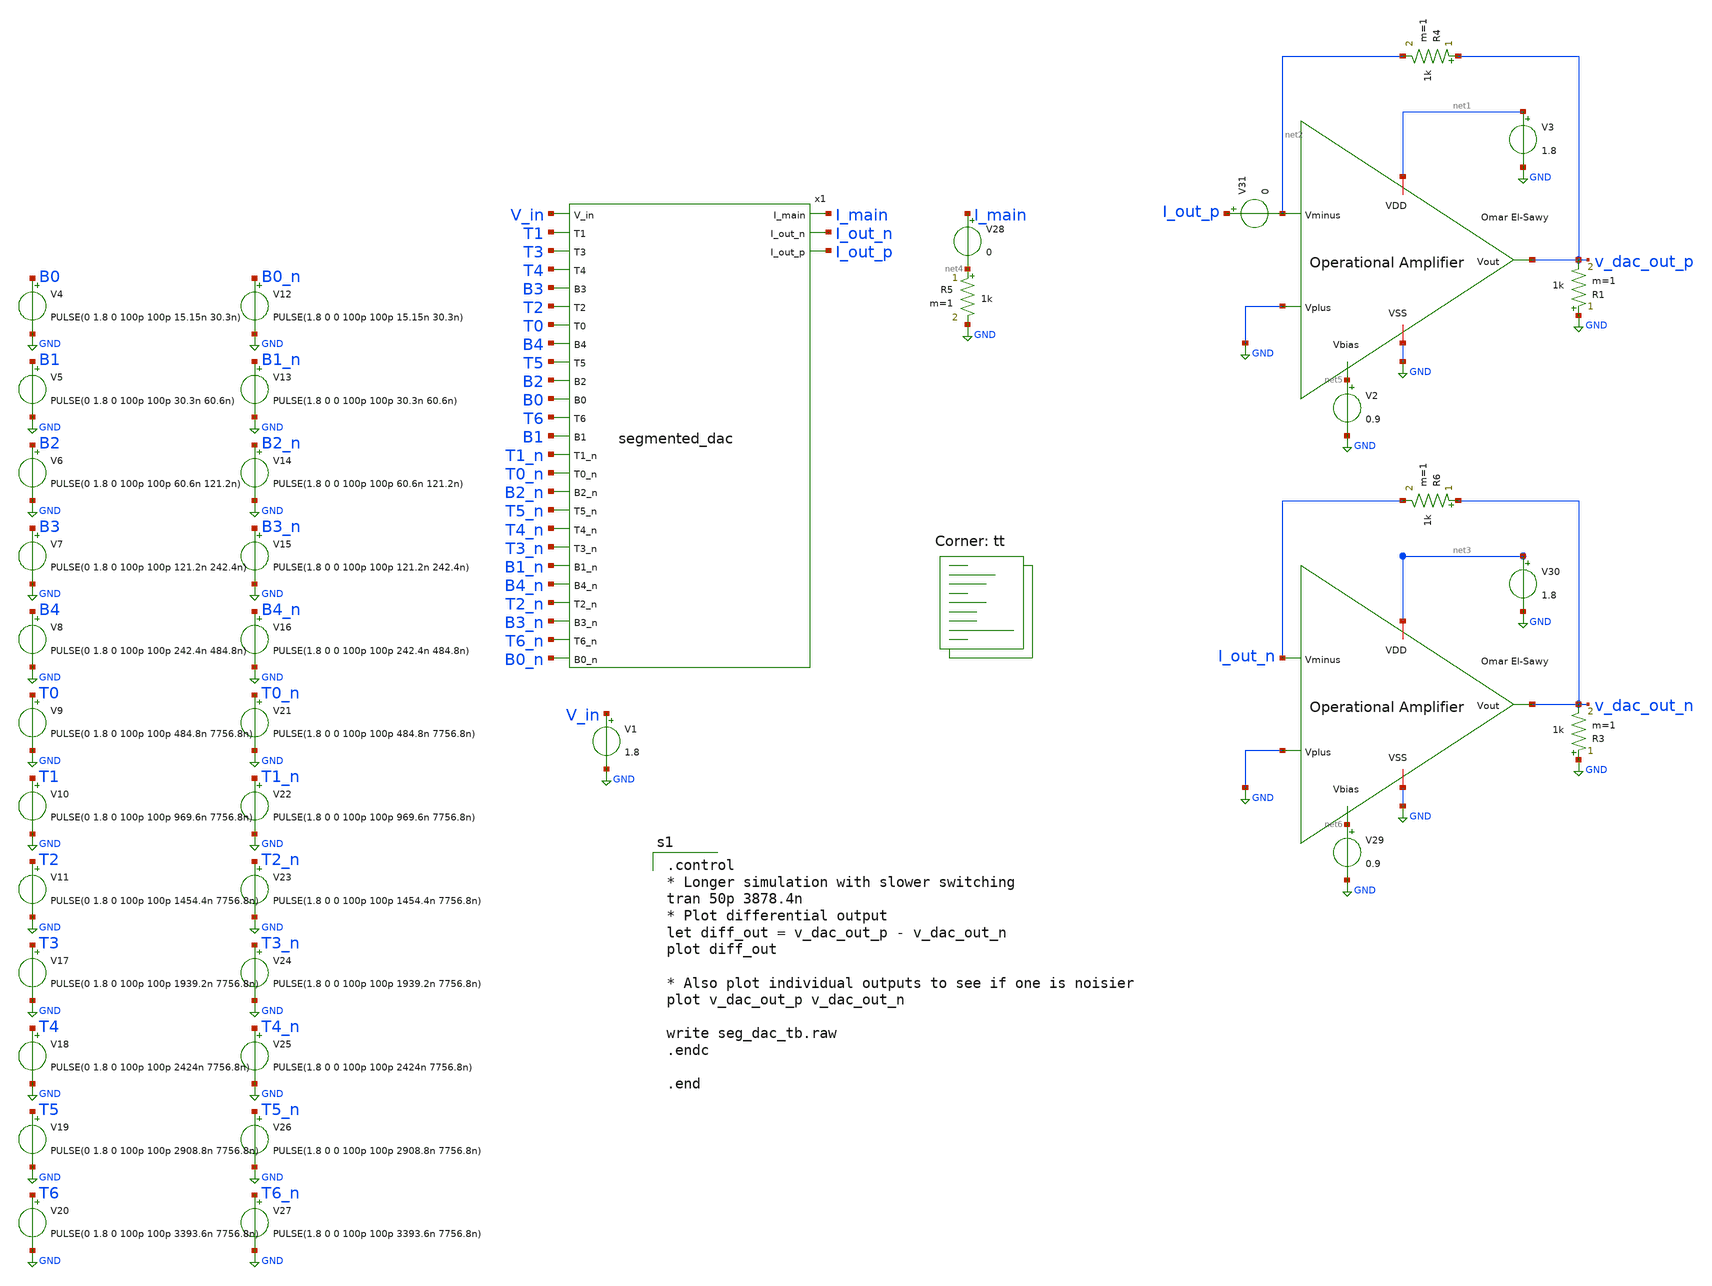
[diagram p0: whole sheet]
** sch_path: analog/schematics/testbenches/seg_dac_tb.sch
**.subckt seg_dac_tb
x1 V_in I_main I_out_n I_out_p T1 T3 T4 B3 T2 T0 B4 T5 B2 B0 T6 B1 T1_n T0_n B2_n T5_n T4_n T3_n
+ B1_n B4_n T2_n B3_n T6_n B0_n segmented_dac
V4 B0 GND PULSE(0 1.8 0 100p 100p 15.15n 30.3n)
V5 B1 GND PULSE(0 1.8 0 100p 100p 30.3n 60.6n)
V6 B2 GND PULSE(0 1.8 0 100p 100p 60.6n 121.2n)
V7 B3 GND PULSE(0 1.8 0 100p 100p 121.2n 242.4n)
V8 B4 GND PULSE(0 1.8 0 100p 100p 242.4n 484.8n)
V9 T0 GND PULSE(0 1.8 0 100p 100p 484.8n 7756.8n)
V10 T1 GND PULSE(0 1.8 0 100p 100p 969.6n 7756.8n)
V11 T2 GND PULSE(0 1.8 0 100p 100p 1454.4n 7756.8n)
V17 T3 GND PULSE(0 1.8 0 100p 100p 1939.2n 7756.8n)
V18 T4 GND PULSE(0 1.8 0 100p 100p 2424n 7756.8n)
V19 T5 GND PULSE(0 1.8 0 100p 100p 2908.8n 7756.8n)
V20 T6 GND PULSE(0 1.8 0 100p 100p 3393.6n 7756.8n)
V12 B0_n GND PULSE(1.8 0 0 100p 100p 15.15n 30.3n)
V13 B1_n GND PULSE(1.8 0 0 100p 100p 30.3n 60.6n)
V14 B2_n GND PULSE(1.8 0 0 100p 100p 60.6n 121.2n)
V15 B3_n GND PULSE(1.8 0 0 100p 100p 121.2n 242.4n)
V16 B4_n GND PULSE(1.8 0 0 100p 100p 242.4n 484.8n)
V21 T0_n GND PULSE(1.8 0 0 100p 100p 484.8n 7756.8n)
V22 T1_n GND PULSE(1.8 0 0 100p 100p 969.6n 7756.8n)
V23 T2_n GND PULSE(1.8 0 0 100p 100p 1454.4n 7756.8n)
V24 T3_n GND PULSE(1.8 0 0 100p 100p 1939.2n 7756.8n)
V25 T4_n GND PULSE(1.8 0 0 100p 100p 2424n 7756.8n)
V26 T5_n GND PULSE(1.8 0 0 100p 100p 2908.8n 7756.8n)
V27 T6_n GND PULSE(1.8 0 0 100p 100p 3393.6n 7756.8n)
R5 net4 GND 1k m=1
x2 net1 v_dac_out_p net2 GND net5 GND OpAmp
V2 net5 GND 0.9
V3 net1 GND 1.8
R4 v_dac_out_p net2 1k m=1
R1 GND v_dac_out_p 1k m=1
x3 net3 v_dac_out_n I_out_n GND net6 GND OpAmp
R6 v_dac_out_n I_out_n 1k m=1
R3 GND v_dac_out_n 1k m=1
V1 V_in GND 1.8
V28 I_main net4 0
V29 net6 GND 0.9
V30 net3 GND 1.8
V31 I_out_p net2 0
**** begin user architecture code
.lib $::SKYWATER_MODELS/sky130.lib.spice tt

.control
* Longer simulation with slower switching
tran 50p 3878.4n
* Plot differential output
let diff_out = v_dac_out_p - v_dac_out_n
plot diff_out

* Also plot individual outputs to see if one is noisier
plot v_dac_out_p v_dac_out_n

write seg_dac_tb.raw
.endc

.end

**** end user architecture code
**.ends

* expanding   symbol:  segmented_dac.sym # of pins=28
** sym_path: analog/schematics/segmented_dac.sym
** sch_path: analog/schematics/segmented_dac.sch
.subckt segmented_dac V_in I_main I_out_n I_out_p T1 T3 T4 B3 T2 T0 B4 T5 B2 B0 T6 B1 T1_n T0_n B2_n
+ T5_n T4_n T3_n B1_n B4_n T2_n B3_n T6_n B0_n
*.ipin B0
*.ipin B0_n
*.ipin B1
*.ipin B2
*.ipin B3
*.ipin B1_n
*.ipin B2_n
*.ipin B3_n
*.ipin B4
*.ipin B4_n
*.ipin T0
*.ipin T1
*.ipin T2
*.ipin T0_n
*.ipin T1_n
*.ipin T2_n
*.opin I_out_p
*.ipin V_in
*.opin I_out_n
*.opin I_main
*.ipin T3
*.ipin T4
*.ipin T5
*.ipin T3_n
*.ipin T4_n
*.ipin T5_n
*.ipin T6
*.ipin T6_n
XM1 net2 net1 V_in V_in sky130_fd_pr__pfet_01v8 L=length W=min_width nf=1 ad='int((nf+1)/2) * W/nf * 0.29'
+ as='int((nf+2)/2) * W/nf * 0.29' pd='2*int((nf+1)/2) * (W/nf + 0.29)' ps='2*int((nf+2)/2) * (W/nf + 0.29)'
+ nrd='0.29 / W' nrs='0.29 / W' sa=0 sb=0 sd=0 mult=32 m=32
XM2 net6 I_main net2 net2 sky130_fd_pr__pfet_01v8 L=length W=min_width nf=1 ad='int((nf+1)/2) * W/nf * 0.29'
+ as='int((nf+2)/2) * W/nf * 0.29' pd='2*int((nf+1)/2) * (W/nf + 0.29)' ps='2*int((nf+2)/2) * (W/nf + 0.29)'
+ nrd='0.29 / W' nrs='0.29 / W' sa=0 sb=0 sd=0 mult=32 m=32
XM3 net1 net1 V_in V_in sky130_fd_pr__pfet_01v8 L=length W=min_width nf=1 ad='int((nf+1)/2) * W/nf * 0.29'
+ as='int((nf+2)/2) * W/nf * 0.29' pd='2*int((nf+1)/2) * (W/nf + 0.29)' ps='2*int((nf+2)/2) * (W/nf + 0.29)'
+ nrd='0.29 / W' nrs='0.29 / W' sa=0 sb=0 sd=0 mult=128 m=128
XM4 I_main I_main net1 net1 sky130_fd_pr__pfet_01v8 L=length W=min_width nf=1 ad='int((nf+1)/2) * W/nf * 0.29'
+ as='int((nf+2)/2) * W/nf * 0.29' pd='2*int((nf+1)/2) * (W/nf + 0.29)' ps='2*int((nf+2)/2) * (W/nf + 0.29)'
+ nrd='0.29 / W' nrs='0.29 / W' sa=0 sb=0 sd=0 mult=128 m=128
XM5 net3 net1 V_in V_in sky130_fd_pr__pfet_01v8 L=length W=min_width nf=1 ad='int((nf+1)/2) * W/nf * 0.29'
+ as='int((nf+2)/2) * W/nf * 0.29' pd='2*int((nf+1)/2) * (W/nf + 0.29)' ps='2*int((nf+2)/2) * (W/nf + 0.29)'
+ nrd='0.29 / W' nrs='0.29 / W' sa=0 sb=0 sd=0 mult=32 m=32
XM6 net7 I_main net3 net3 sky130_fd_pr__pfet_01v8 L=length W=min_width nf=1 ad='int((nf+1)/2) * W/nf * 0.29'
+ as='int((nf+2)/2) * W/nf * 0.29' pd='2*int((nf+1)/2) * (W/nf + 0.29)' ps='2*int((nf+2)/2) * (W/nf + 0.29)'
+ nrd='0.29 / W' nrs='0.29 / W' sa=0 sb=0 sd=0 mult=32 m=32
XM7 net4 net1 V_in V_in sky130_fd_pr__pfet_01v8 L=length W=min_width nf=1 ad='int((nf+1)/2) * W/nf * 0.29'
+ as='int((nf+2)/2) * W/nf * 0.29' pd='2*int((nf+1)/2) * (W/nf + 0.29)' ps='2*int((nf+2)/2) * (W/nf + 0.29)'
+ nrd='0.29 / W' nrs='0.29 / W' sa=0 sb=0 sd=0 mult=32 m=32
XM8 net8 I_main net4 net4 sky130_fd_pr__pfet_01v8 L=length W=min_width nf=1 ad='int((nf+1)/2) * W/nf * 0.29'
+ as='int((nf+2)/2) * W/nf * 0.29' pd='2*int((nf+1)/2) * (W/nf + 0.29)' ps='2*int((nf+2)/2) * (W/nf + 0.29)'
+ nrd='0.29 / W' nrs='0.29 / W' sa=0 sb=0 sd=0 mult=32 m=32
XM9 net5 net1 V_in V_in sky130_fd_pr__pfet_01v8 L=length W=min_width nf=1 ad='int((nf+1)/2) * W/nf * 0.29'
+ as='int((nf+2)/2) * W/nf * 0.29' pd='2*int((nf+1)/2) * (W/nf + 0.29)' ps='2*int((nf+2)/2) * (W/nf + 0.29)'
+ nrd='0.29 / W' nrs='0.29 / W' sa=0 sb=0 sd=0 mult=16 m=16
XM10 net9 I_main net5 net5 sky130_fd_pr__pfet_01v8 L=length W=min_width nf=1 ad='int((nf+1)/2) * W/nf * 0.29'
+ as='int((nf+2)/2) * W/nf * 0.29' pd='2*int((nf+1)/2) * (W/nf + 0.29)' ps='2*int((nf+2)/2) * (W/nf + 0.29)'
+ nrd='0.29 / W' nrs='0.29 / W' sa=0 sb=0 sd=0 mult=16 m=16
XM12 I_out_p T2 net6 net6 sky130_fd_pr__pfet_01v8 L=length W=min_width*switch_multiplier nf=1 ad='int((nf+1)/2) * W/nf * 0.29'
+ as='int((nf+2)/2) * W/nf * 0.29' pd='2*int((nf+1)/2) * (W/nf + 0.29)' ps='2*int((nf+2)/2) * (W/nf + 0.29)'
+ nrd='0.29 / W' nrs='0.29 / W' sa=0 sb=0 sd=0 mult=32 m=32
XM13 I_out_n T2_n net6 net6 sky130_fd_pr__pfet_01v8 L=length W=min_width*switch_multiplier nf=1 ad='int((nf+1)/2) * W/nf * 0.29'
+ as='int((nf+2)/2) * W/nf * 0.29' pd='2*int((nf+1)/2) * (W/nf + 0.29)' ps='2*int((nf+2)/2) * (W/nf + 0.29)'
+ nrd='0.29 / W' nrs='0.29 / W' sa=0 sb=0 sd=0 mult=32 m=32
XM14 I_out_p T1 net7 net7 sky130_fd_pr__pfet_01v8 L=length W=min_width*switch_multiplier nf=1 ad='int((nf+1)/2) * W/nf * 0.29'
+ as='int((nf+2)/2) * W/nf * 0.29' pd='2*int((nf+1)/2) * (W/nf + 0.29)' ps='2*int((nf+2)/2) * (W/nf + 0.29)'
+ nrd='0.29 / W' nrs='0.29 / W' sa=0 sb=0 sd=0 mult=32 m=32
XM15 I_out_n T1_n net7 net7 sky130_fd_pr__pfet_01v8 L=length W=min_width*switch_multiplier nf=1 ad='int((nf+1)/2) * W/nf * 0.29'
+ as='int((nf+2)/2) * W/nf * 0.29' pd='2*int((nf+1)/2) * (W/nf + 0.29)' ps='2*int((nf+2)/2) * (W/nf + 0.29)'
+ nrd='0.29 / W' nrs='0.29 / W' sa=0 sb=0 sd=0 mult=32 m=32
XM16 I_out_p T0 net8 net8 sky130_fd_pr__pfet_01v8 L=length W=min_width*switch_multiplier nf=1 ad='int((nf+1)/2) * W/nf * 0.29'
+ as='int((nf+2)/2) * W/nf * 0.29' pd='2*int((nf+1)/2) * (W/nf + 0.29)' ps='2*int((nf+2)/2) * (W/nf + 0.29)'
+ nrd='0.29 / W' nrs='0.29 / W' sa=0 sb=0 sd=0 mult=32 m=32
XM17 I_out_n T0_n net8 net8 sky130_fd_pr__pfet_01v8 L=length W=min_width*switch_multiplier nf=1 ad='int((nf+1)/2) * W/nf * 0.29'
+ as='int((nf+2)/2) * W/nf * 0.29' pd='2*int((nf+1)/2) * (W/nf + 0.29)' ps='2*int((nf+2)/2) * (W/nf + 0.29)'
+ nrd='0.29 / W' nrs='0.29 / W' sa=0 sb=0 sd=0 mult=32 m=32
XM18 I_out_p B4 net9 net9 sky130_fd_pr__pfet_01v8 L=length W=min_width*switch_multiplier nf=1 ad='int((nf+1)/2) * W/nf * 0.29'
+ as='int((nf+2)/2) * W/nf * 0.29' pd='2*int((nf+1)/2) * (W/nf + 0.29)' ps='2*int((nf+2)/2) * (W/nf + 0.29)'
+ nrd='0.29 / W' nrs='0.29 / W' sa=0 sb=0 sd=0 mult=16 m=16
XM19 I_out_n B4_n net9 net9 sky130_fd_pr__pfet_01v8 L=length W=min_width*switch_multiplier nf=1 ad='int((nf+1)/2) * W/nf * 0.29'
+ as='int((nf+2)/2) * W/nf * 0.29' pd='2*int((nf+1)/2) * (W/nf + 0.29)' ps='2*int((nf+2)/2) * (W/nf + 0.29)'
+ nrd='0.29 / W' nrs='0.29 / W' sa=0 sb=0 sd=0 mult=16 m=16
XM11 net10 net1 V_in V_in sky130_fd_pr__pfet_01v8 L=length W=min_width nf=1 ad='int((nf+1)/2) * W/nf * 0.29'
+ as='int((nf+2)/2) * W/nf * 0.29' pd='2*int((nf+1)/2) * (W/nf + 0.29)' ps='2*int((nf+2)/2) * (W/nf + 0.29)'
+ nrd='0.29 / W' nrs='0.29 / W' sa=0 sb=0 sd=0 mult=8 m=8
XM20 net14 I_main net10 net10 sky130_fd_pr__pfet_01v8 L=length W=min_width nf=1 ad='int((nf+1)/2) * W/nf * 0.29'
+ as='int((nf+2)/2) * W/nf * 0.29' pd='2*int((nf+1)/2) * (W/nf + 0.29)' ps='2*int((nf+2)/2) * (W/nf + 0.29)'
+ nrd='0.29 / W' nrs='0.29 / W' sa=0 sb=0 sd=0 mult=8 m=8
XM21 net11 net1 V_in V_in sky130_fd_pr__pfet_01v8 L=length W=min_width nf=1 ad='int((nf+1)/2) * W/nf * 0.29'
+ as='int((nf+2)/2) * W/nf * 0.29' pd='2*int((nf+1)/2) * (W/nf + 0.29)' ps='2*int((nf+2)/2) * (W/nf + 0.29)'
+ nrd='0.29 / W' nrs='0.29 / W' sa=0 sb=0 sd=0 mult=4 m=4
XM22 net15 I_main net11 net11 sky130_fd_pr__pfet_01v8 L=length W=min_width nf=1 ad='int((nf+1)/2) * W/nf * 0.29'
+ as='int((nf+2)/2) * W/nf * 0.29' pd='2*int((nf+1)/2) * (W/nf + 0.29)' ps='2*int((nf+2)/2) * (W/nf + 0.29)'
+ nrd='0.29 / W' nrs='0.29 / W' sa=0 sb=0 sd=0 mult=4 m=4
XM23 net12 net1 V_in V_in sky130_fd_pr__pfet_01v8 L=length W=min_width nf=1 ad='int((nf+1)/2) * W/nf * 0.29'
+ as='int((nf+2)/2) * W/nf * 0.29' pd='2*int((nf+1)/2) * (W/nf + 0.29)' ps='2*int((nf+2)/2) * (W/nf + 0.29)'
+ nrd='0.29 / W' nrs='0.29 / W' sa=0 sb=0 sd=0 mult=2 m=2
XM24 net16 I_main net12 net12 sky130_fd_pr__pfet_01v8 L=length W=min_width nf=1 ad='int((nf+1)/2) * W/nf * 0.29'
+ as='int((nf+2)/2) * W/nf * 0.29' pd='2*int((nf+1)/2) * (W/nf + 0.29)' ps='2*int((nf+2)/2) * (W/nf + 0.29)'
+ nrd='0.29 / W' nrs='0.29 / W' sa=0 sb=0 sd=0 mult=2 m=2
XM25 net13 net1 V_in V_in sky130_fd_pr__pfet_01v8 L=length W=min_width nf=1 ad='int((nf+1)/2) * W/nf * 0.29'
+ as='int((nf+2)/2) * W/nf * 0.29' pd='2*int((nf+1)/2) * (W/nf + 0.29)' ps='2*int((nf+2)/2) * (W/nf + 0.29)'
+ nrd='0.29 / W' nrs='0.29 / W' sa=0 sb=0 sd=0 mult=1 m=1
XM26 net17 I_main net13 net13 sky130_fd_pr__pfet_01v8 L=length W=min_width nf=1 ad='int((nf+1)/2) * W/nf * 0.29'
+ as='int((nf+2)/2) * W/nf * 0.29' pd='2*int((nf+1)/2) * (W/nf + 0.29)' ps='2*int((nf+2)/2) * (W/nf + 0.29)'
+ nrd='0.29 / W' nrs='0.29 / W' sa=0 sb=0 sd=0 mult=1 m=1
XM27 I_out_p B3 net14 net14 sky130_fd_pr__pfet_01v8 L=length W=min_width*switch_multiplier nf=1 ad='int((nf+1)/2) * W/nf * 0.29'
+ as='int((nf+2)/2) * W/nf * 0.29' pd='2*int((nf+1)/2) * (W/nf + 0.29)' ps='2*int((nf+2)/2) * (W/nf + 0.29)'
+ nrd='0.29 / W' nrs='0.29 / W' sa=0 sb=0 sd=0 mult=8 m=8
XM28 I_out_n B3_n net14 net14 sky130_fd_pr__pfet_01v8 L=length W=min_width*switch_multiplier nf=1 ad='int((nf+1)/2) * W/nf * 0.29'
+ as='int((nf+2)/2) * W/nf * 0.29' pd='2*int((nf+1)/2) * (W/nf + 0.29)' ps='2*int((nf+2)/2) * (W/nf + 0.29)'
+ nrd='0.29 / W' nrs='0.29 / W' sa=0 sb=0 sd=0 mult=8 m=8
XM29 I_out_p B2 net15 net15 sky130_fd_pr__pfet_01v8 L=length W=min_width*switch_multiplier nf=1 ad='int((nf+1)/2) * W/nf * 0.29'
+ as='int((nf+2)/2) * W/nf * 0.29' pd='2*int((nf+1)/2) * (W/nf + 0.29)' ps='2*int((nf+2)/2) * (W/nf + 0.29)'
+ nrd='0.29 / W' nrs='0.29 / W' sa=0 sb=0 sd=0 mult=4 m=4
XM30 I_out_n B2_n net15 net15 sky130_fd_pr__pfet_01v8 L=length W=min_width*switch_multiplier nf=1 ad='int((nf+1)/2) * W/nf * 0.29'
+ as='int((nf+2)/2) * W/nf * 0.29' pd='2*int((nf+1)/2) * (W/nf + 0.29)' ps='2*int((nf+2)/2) * (W/nf + 0.29)'
+ nrd='0.29 / W' nrs='0.29 / W' sa=0 sb=0 sd=0 mult=4 m=4
XM31 I_out_p B1 net16 net16 sky130_fd_pr__pfet_01v8 L=length W=min_width*switch_multiplier nf=1 ad='int((nf+1)/2) * W/nf * 0.29'
+ as='int((nf+2)/2) * W/nf * 0.29' pd='2*int((nf+1)/2) * (W/nf + 0.29)' ps='2*int((nf+2)/2) * (W/nf + 0.29)'
+ nrd='0.29 / W' nrs='0.29 / W' sa=0 sb=0 sd=0 mult=2 m=2
XM32 I_out_n B1_n net16 net16 sky130_fd_pr__pfet_01v8 L=length W=min_width*switch_multiplier nf=1 ad='int((nf+1)/2) * W/nf * 0.29'
+ as='int((nf+2)/2) * W/nf * 0.29' pd='2*int((nf+1)/2) * (W/nf + 0.29)' ps='2*int((nf+2)/2) * (W/nf + 0.29)'
+ nrd='0.29 / W' nrs='0.29 / W' sa=0 sb=0 sd=0 mult=2 m=2
XM33 I_out_p B0 net17 net17 sky130_fd_pr__pfet_01v8 L=length W=min_width*switch_multiplier nf=1 ad='int((nf+1)/2) * W/nf * 0.29'
+ as='int((nf+2)/2) * W/nf * 0.29' pd='2*int((nf+1)/2) * (W/nf + 0.29)' ps='2*int((nf+2)/2) * (W/nf + 0.29)'
+ nrd='0.29 / W' nrs='0.29 / W' sa=0 sb=0 sd=0 mult=1 m=1
XM34 I_out_n B0_n net17 net17 sky130_fd_pr__pfet_01v8 L=length W=min_width*switch_multiplier nf=1 ad='int((nf+1)/2) * W/nf * 0.29'
+ as='int((nf+2)/2) * W/nf * 0.29' pd='2*int((nf+1)/2) * (W/nf + 0.29)' ps='2*int((nf+2)/2) * (W/nf + 0.29)'
+ nrd='0.29 / W' nrs='0.29 / W' sa=0 sb=0 sd=0 mult=1 m=1
**** begin user architecture code

.param min_width=0.42
.param switch_multiplier=1
.param length=0.425

**** end user architecture code
XM35 net18 net1 V_in V_in sky130_fd_pr__pfet_01v8 L=length W=min_width nf=1 ad='int((nf+1)/2) * W/nf * 0.29'
+ as='int((nf+2)/2) * W/nf * 0.29' pd='2*int((nf+1)/2) * (W/nf + 0.29)' ps='2*int((nf+2)/2) * (W/nf + 0.29)'
+ nrd='0.29 / W' nrs='0.29 / W' sa=0 sb=0 sd=0 mult=32 m=32
XM36 net21 I_main net18 net18 sky130_fd_pr__pfet_01v8 L=length W=min_width nf=1 ad='int((nf+1)/2) * W/nf * 0.29'
+ as='int((nf+2)/2) * W/nf * 0.29' pd='2*int((nf+1)/2) * (W/nf + 0.29)' ps='2*int((nf+2)/2) * (W/nf + 0.29)'
+ nrd='0.29 / W' nrs='0.29 / W' sa=0 sb=0 sd=0 mult=32 m=32
XM37 net19 net1 V_in V_in sky130_fd_pr__pfet_01v8 L=length W=min_width nf=1 ad='int((nf+1)/2) * W/nf * 0.29'
+ as='int((nf+2)/2) * W/nf * 0.29' pd='2*int((nf+1)/2) * (W/nf + 0.29)' ps='2*int((nf+2)/2) * (W/nf + 0.29)'
+ nrd='0.29 / W' nrs='0.29 / W' sa=0 sb=0 sd=0 mult=32 m=32
XM38 net22 I_main net19 net19 sky130_fd_pr__pfet_01v8 L=length W=min_width nf=1 ad='int((nf+1)/2) * W/nf * 0.29'
+ as='int((nf+2)/2) * W/nf * 0.29' pd='2*int((nf+1)/2) * (W/nf + 0.29)' ps='2*int((nf+2)/2) * (W/nf + 0.29)'
+ nrd='0.29 / W' nrs='0.29 / W' sa=0 sb=0 sd=0 mult=32 m=32
XM39 net20 net1 V_in V_in sky130_fd_pr__pfet_01v8 L=length W=min_width nf=1 ad='int((nf+1)/2) * W/nf * 0.29'
+ as='int((nf+2)/2) * W/nf * 0.29' pd='2*int((nf+1)/2) * (W/nf + 0.29)' ps='2*int((nf+2)/2) * (W/nf + 0.29)'
+ nrd='0.29 / W' nrs='0.29 / W' sa=0 sb=0 sd=0 mult=32 m=32
XM40 net23 I_main net20 net20 sky130_fd_pr__pfet_01v8 L=length W=min_width nf=1 ad='int((nf+1)/2) * W/nf * 0.29'
+ as='int((nf+2)/2) * W/nf * 0.29' pd='2*int((nf+1)/2) * (W/nf + 0.29)' ps='2*int((nf+2)/2) * (W/nf + 0.29)'
+ nrd='0.29 / W' nrs='0.29 / W' sa=0 sb=0 sd=0 mult=32 m=32
XM41 I_out_p T5 net21 net21 sky130_fd_pr__pfet_01v8 L=length W=min_width*switch_multiplier nf=1 ad='int((nf+1)/2) * W/nf * 0.29'
+ as='int((nf+2)/2) * W/nf * 0.29' pd='2*int((nf+1)/2) * (W/nf + 0.29)' ps='2*int((nf+2)/2) * (W/nf + 0.29)'
+ nrd='0.29 / W' nrs='0.29 / W' sa=0 sb=0 sd=0 mult=32 m=32
XM42 I_out_n T5_n net21 net21 sky130_fd_pr__pfet_01v8 L=length W=min_width*switch_multiplier nf=1 ad='int((nf+1)/2) * W/nf * 0.29'
+ as='int((nf+2)/2) * W/nf * 0.29' pd='2*int((nf+1)/2) * (W/nf + 0.29)' ps='2*int((nf+2)/2) * (W/nf + 0.29)'
+ nrd='0.29 / W' nrs='0.29 / W' sa=0 sb=0 sd=0 mult=32 m=32
XM43 I_out_p T4 net22 net22 sky130_fd_pr__pfet_01v8 L=length W=min_width*switch_multiplier nf=1 ad='int((nf+1)/2) * W/nf * 0.29'
+ as='int((nf+2)/2) * W/nf * 0.29' pd='2*int((nf+1)/2) * (W/nf + 0.29)' ps='2*int((nf+2)/2) * (W/nf + 0.29)'
+ nrd='0.29 / W' nrs='0.29 / W' sa=0 sb=0 sd=0 mult=32 m=32
XM44 I_out_n T4_n net22 net22 sky130_fd_pr__pfet_01v8 L=length W=min_width*switch_multiplier nf=1 ad='int((nf+1)/2) * W/nf * 0.29'
+ as='int((nf+2)/2) * W/nf * 0.29' pd='2*int((nf+1)/2) * (W/nf + 0.29)' ps='2*int((nf+2)/2) * (W/nf + 0.29)'
+ nrd='0.29 / W' nrs='0.29 / W' sa=0 sb=0 sd=0 mult=32 m=32
XM45 I_out_p T3 net23 net23 sky130_fd_pr__pfet_01v8 L=length W=min_width*switch_multiplier nf=1 ad='int((nf+1)/2) * W/nf * 0.29'
+ as='int((nf+2)/2) * W/nf * 0.29' pd='2*int((nf+1)/2) * (W/nf + 0.29)' ps='2*int((nf+2)/2) * (W/nf + 0.29)'
+ nrd='0.29 / W' nrs='0.29 / W' sa=0 sb=0 sd=0 mult=32 m=32
XM46 I_out_n T3_n net23 net23 sky130_fd_pr__pfet_01v8 L=length W=min_width*switch_multiplier nf=1 ad='int((nf+1)/2) * W/nf * 0.29'
+ as='int((nf+2)/2) * W/nf * 0.29' pd='2*int((nf+1)/2) * (W/nf + 0.29)' ps='2*int((nf+2)/2) * (W/nf + 0.29)'
+ nrd='0.29 / W' nrs='0.29 / W' sa=0 sb=0 sd=0 mult=32 m=32
XM47 net24 net1 V_in V_in sky130_fd_pr__pfet_01v8 L=length W=min_width nf=1 ad='int((nf+1)/2) * W/nf * 0.29'
+ as='int((nf+2)/2) * W/nf * 0.29' pd='2*int((nf+1)/2) * (W/nf + 0.29)' ps='2*int((nf+2)/2) * (W/nf + 0.29)'
+ nrd='0.29 / W' nrs='0.29 / W' sa=0 sb=0 sd=0 mult=32 m=32
XM48 net25 I_main net24 net24 sky130_fd_pr__pfet_01v8 L=length W=min_width nf=1 ad='int((nf+1)/2) * W/nf * 0.29'
+ as='int((nf+2)/2) * W/nf * 0.29' pd='2*int((nf+1)/2) * (W/nf + 0.29)' ps='2*int((nf+2)/2) * (W/nf + 0.29)'
+ nrd='0.29 / W' nrs='0.29 / W' sa=0 sb=0 sd=0 mult=32 m=32
XM49 I_out_p T6 net25 net25 sky130_fd_pr__pfet_01v8 L=length W=min_width*switch_multiplier nf=1 ad='int((nf+1)/2) * W/nf * 0.29'
+ as='int((nf+2)/2) * W/nf * 0.29' pd='2*int((nf+1)/2) * (W/nf + 0.29)' ps='2*int((nf+2)/2) * (W/nf + 0.29)'
+ nrd='0.29 / W' nrs='0.29 / W' sa=0 sb=0 sd=0 mult=32 m=32
XM50 I_out_n T6_n net25 net25 sky130_fd_pr__pfet_01v8 L=length W=min_width*switch_multiplier nf=1 ad='int((nf+1)/2) * W/nf * 0.29'
+ as='int((nf+2)/2) * W/nf * 0.29' pd='2*int((nf+1)/2) * (W/nf + 0.29)' ps='2*int((nf+2)/2) * (W/nf + 0.29)'
+ nrd='0.29 / W' nrs='0.29 / W' sa=0 sb=0 sd=0 mult=32 m=32
.ends


* expanding   symbol:  OpAmps/template/OpAmp.sym # of pins=6
** sym_path: OpAmps/template/OpAmp.sym
** sch_path: OpAmps/template/OpAmp.sch
.subckt OpAmp VDD Vout Vminus Vplus Vbias VSS
*.ipin Vplus
*.ipin Vminus
*.iopin VDD
*.iopin VSS
*.ipin Vbias
*.opin Vout
XM1 net2 Vminus net1 VSS sky130_fd_pr__nfet_01v8 L=0.15 W=16 nf=1 ad='int((nf+1)/2) * W/nf * 0.29' as='int((nf+2)/2) * W/nf * 0.29'
+ pd='2*int((nf+1)/2) * (W/nf + 0.29)' ps='2*int((nf+2)/2) * (W/nf + 0.29)' nrd='0.29 / W' nrs='0.29 / W'
+ sa=0 sb=0 sd=0 mult=1 m=1
XM2 net3 Vplus net1 VSS sky130_fd_pr__nfet_01v8 L=0.15 W=16 nf=1 ad='int((nf+1)/2) * W/nf * 0.29' as='int((nf+2)/2) * W/nf * 0.29'
+ pd='2*int((nf+1)/2) * (W/nf + 0.29)' ps='2*int((nf+2)/2) * (W/nf + 0.29)' nrd='0.29 / W' nrs='0.29 / W'
+ sa=0 sb=0 sd=0 mult=1 m=1
XM3 net2 net2 VDD VDD sky130_fd_pr__pfet_01v8 L=0.4 W=1 nf=1 ad='int((nf+1)/2) * W/nf * 0.29' as='int((nf+2)/2) * W/nf * 0.29'
+ pd='2*int((nf+1)/2) * (W/nf + 0.29)' ps='2*int((nf+2)/2) * (W/nf + 0.29)' nrd='0.29 / W' nrs='0.29 / W'
+ sa=0 sb=0 sd=0 mult=1 m=1
XM4 net3 net2 VDD VDD sky130_fd_pr__pfet_01v8 L=0.4 W=1 nf=1 ad='int((nf+1)/2) * W/nf * 0.29' as='int((nf+2)/2) * W/nf * 0.29'
+ pd='2*int((nf+1)/2) * (W/nf + 0.29)' ps='2*int((nf+2)/2) * (W/nf + 0.29)' nrd='0.29 / W' nrs='0.29 / W'
+ sa=0 sb=0 sd=0 mult=1 m=1
XM5 net1 Vbias VSS VSS sky130_fd_pr__nfet_01v8 L=0.30 W=2 nf=1 ad='int((nf+1)/2) * W/nf * 0.29' as='int((nf+2)/2) * W/nf * 0.29'
+ pd='2*int((nf+1)/2) * (W/nf + 0.29)' ps='2*int((nf+2)/2) * (W/nf + 0.29)' nrd='0.29 / W' nrs='0.29 / W'
+ sa=0 sb=0 sd=0 mult=1 m=1
XM6 Vout net3 VDD VDD sky130_fd_pr__pfet_01v8 L=0.40 W=1 nf=1 ad='int((nf+1)/2) * W/nf * 0.29' as='int((nf+2)/2) * W/nf * 0.29'
+ pd='2*int((nf+1)/2) * (W/nf + 0.29)' ps='2*int((nf+2)/2) * (W/nf + 0.29)' nrd='0.29 / W' nrs='0.29 / W'
+ sa=0 sb=0 sd=0 mult=1 m=1
XC1 Vout net3 sky130_fd_pr__cap_mim_m3_1 W=1 L=1 MF=1 m=1
XM7 Vout Vbias VSS VSS sky130_fd_pr__nfet_01v8 L=0.3 W=1 nf=1 ad='int((nf+1)/2) * W/nf * 0.29' as='int((nf+2)/2) * W/nf * 0.29'
+ pd='2*int((nf+1)/2) * (W/nf + 0.29)' ps='2*int((nf+2)/2) * (W/nf + 0.29)' nrd='0.29 / W' nrs='0.29 / W'
+ sa=0 sb=0 sd=0 mult=1 m=1
.ends

.GLOBAL GND
.GLOBAL VDD
.GLOBAL VSS
.end
